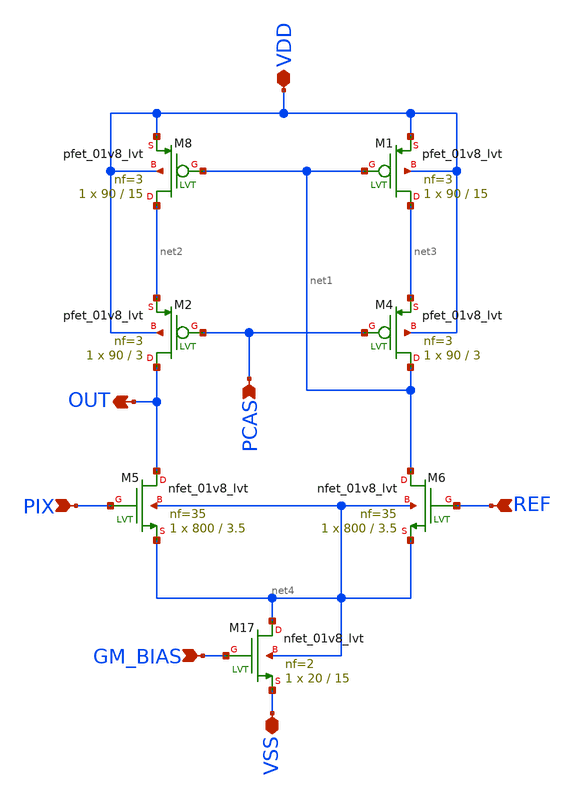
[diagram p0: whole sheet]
** sch_path: xschem/diffamp/diffamp.sch
**.subckt diffamp PCAS PIX REF GM_BIAS OUT VSS VDD
*.ipin PCAS
*.ipin PIX
*.ipin REF
*.ipin GM_BIAS
*.opin OUT
*.iopin VSS
*.iopin VDD
XM17 net4 GM_BIAS VSS net4 sky130_fd_pr__nfet_01v8_lvt L=15 W=20 nf=2 ad='int((2 + 1)/2) * 20 / 2 * 0.29'
+ as='int((2 + 2)/2) * 20 / 2 * 0.29' pd='2*int((2 + 1)/2) * (20 / 2 + 0.29)' ps='2*int((2 + 2)/2) * (20 / 2 + 0.29)'
+ nrd='0.29 / 20 ' nrs='0.29 / 20 ' sa=0 sb=0 sd=0 mult=1 m=1
XM8 net2 net1 VDD VDD sky130_fd_pr__pfet_01v8_lvt L=15 W=90 nf=3 ad='int((3 + 1)/2) * 90 / 3 * 0.29'
+ as='int((3 + 2)/2) * 90 / 3 * 0.29' pd='2*int((3 + 1)/2) * (90 / 3 + 0.29)' ps='2*int((3 + 2)/2) * (90 / 3 + 0.29)'
+ nrd='0.29 / 90 ' nrs='0.29 / 90 ' sa=0 sb=0 sd=0 mult=1 m=1
XM1 net3 net1 VDD VDD sky130_fd_pr__pfet_01v8_lvt L=15 W=90 nf=3 ad='int((3 + 1)/2) * 90 / 3 * 0.29'
+ as='int((3 + 2)/2) * 90 / 3 * 0.29' pd='2*int((3 + 1)/2) * (90 / 3 + 0.29)' ps='2*int((3 + 2)/2) * (90 / 3 + 0.29)'
+ nrd='0.29 / 90 ' nrs='0.29 / 90 ' sa=0 sb=0 sd=0 mult=1 m=1
XM2 OUT PCAS net2 VDD sky130_fd_pr__pfet_01v8_lvt L=3 W=90 nf=3 ad='int((3 + 1)/2) * 90 / 3 * 0.29' as='int((3 + 2)/2) * 90 / 3 * 0.29'
+ pd='2*int((3 + 1)/2) * (90 / 3 + 0.29)' ps='2*int((3 + 2)/2) * (90 / 3 + 0.29)' nrd='0.29 / 90 ' nrs='0.29 / 90 '
+ sa=0 sb=0 sd=0 mult=1 m=1
XM4 net1 PCAS net3 VDD sky130_fd_pr__pfet_01v8_lvt L=3 W=90 nf=3 ad='int((3 + 1)/2) * 90 / 3 * 0.29'
+ as='int((3 + 2)/2) * 90 / 3 * 0.29' pd='2*int((3 + 1)/2) * (90 / 3 + 0.29)' ps='2*int((3 + 2)/2) * (90 / 3 + 0.29)'
+ nrd='0.29 / 90 ' nrs='0.29 / 90 ' sa=0 sb=0 sd=0 mult=1 m=1
XM5 OUT PIX net4 net4 sky130_fd_pr__nfet_01v8_lvt L=3.5 W=800 nf=35 ad='int((35 + 1)/2) * 800 / 35 * 0.29'
+ as='int((35 + 2)/2) * 800 / 35 * 0.29' pd='2*int((35 + 1)/2) * (800 / 35 + 0.29)' ps='2*int((35 + 2)/2) * (800 / 35 + 0.29)'
+ nrd='0.29 / 800 ' nrs='0.29 / 800 ' sa=0 sb=0 sd=0 mult=1 m=1
XM6 net1 REF net4 net4 sky130_fd_pr__nfet_01v8_lvt L=3.5 W=800 nf=35 ad='int((35 + 1)/2) * 800 / 35 * 0.29'
+ as='int((35 + 2)/2) * 800 / 35 * 0.29' pd='2*int((35 + 1)/2) * (800 / 35 + 0.29)' ps='2*int((35 + 2)/2) * (800 / 35 + 0.29)'
+ nrd='0.29 / 800 ' nrs='0.29 / 800 ' sa=0 sb=0 sd=0 mult=1 m=1
**.ends
.end
